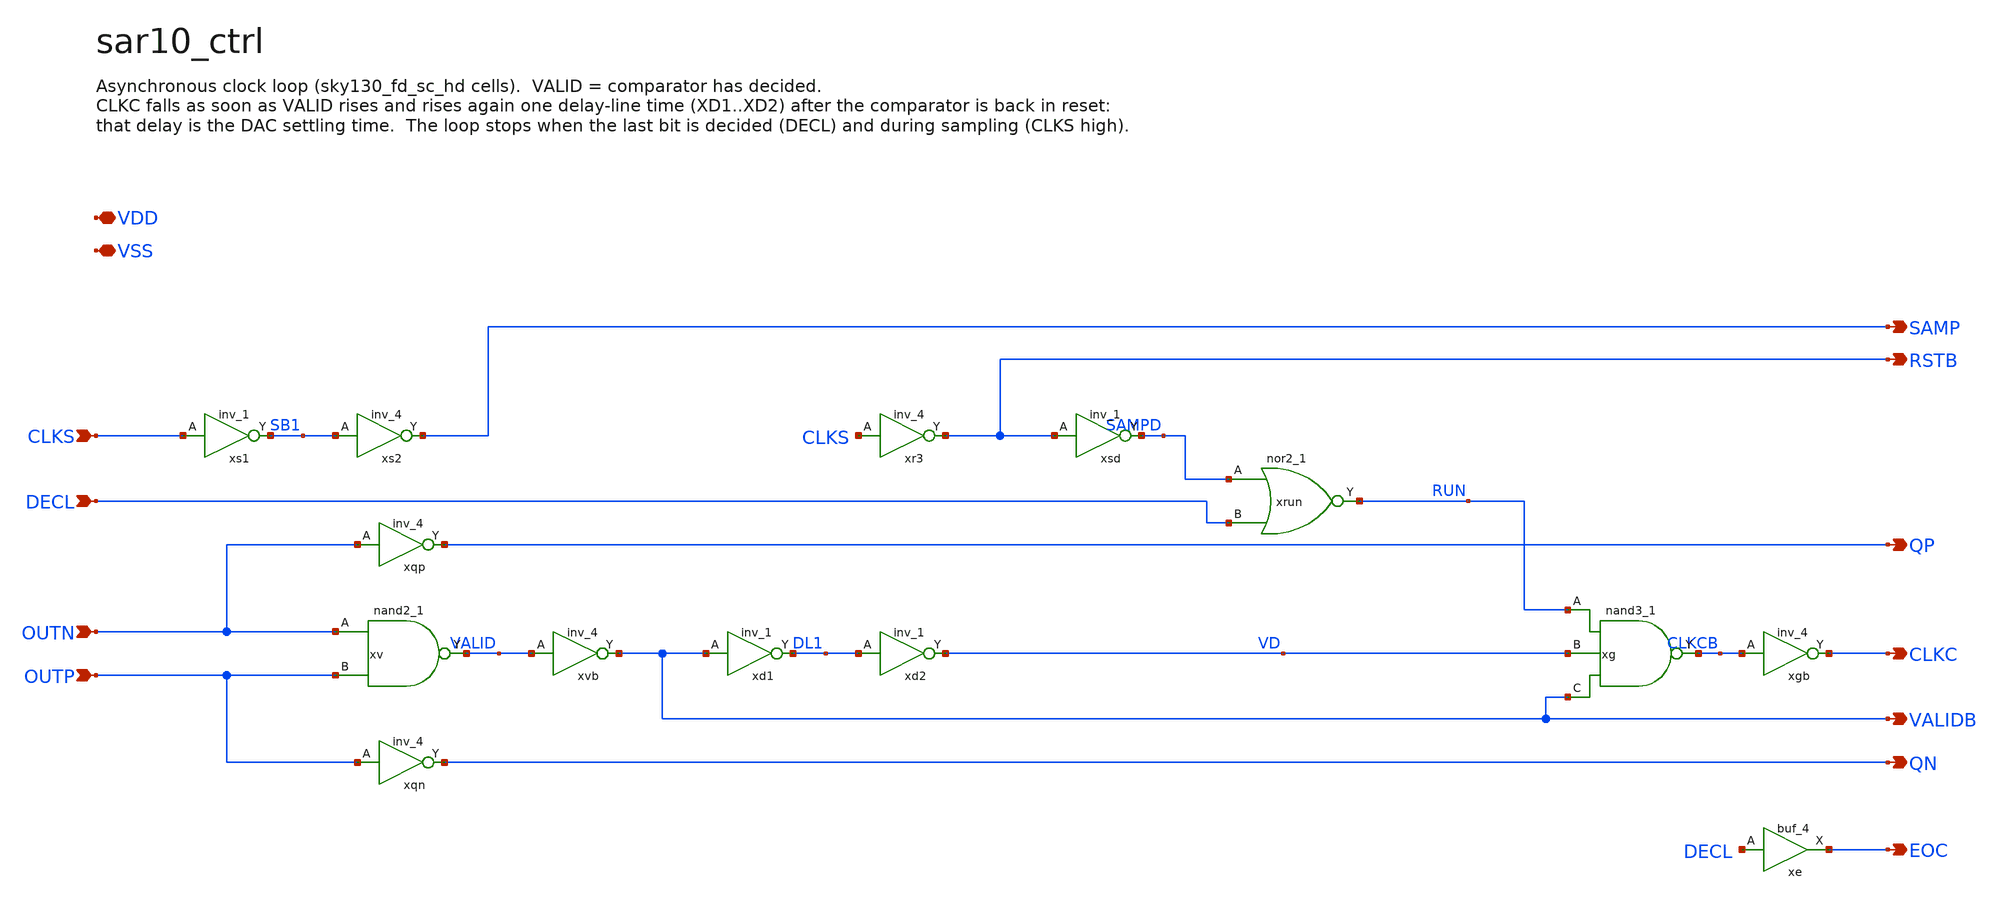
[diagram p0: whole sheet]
** sch_path: xschem/sar10_ctrl.sch
**.subckt sar10_ctrl CLKS DECL OUTN OUTP SAMP RSTB QP CLKC VALIDB QN EOC VDD VSS
*.ipin CLKS
*.ipin DECL
*.ipin OUTN
*.ipin OUTP
*.opin SAMP
*.opin RSTB
*.opin QP
*.opin CLKC
*.opin VALIDB
*.opin QN
*.opin EOC
*.iopin VDD
*.iopin VSS
xs1 CLKS VSS VSS VDD VDD SB1 sky130_fd_sc_hd__inv_1
xs2 SB1 VSS VSS VDD VDD SAMP sky130_fd_sc_hd__inv_4
xr3 CLKS VSS VSS VDD VDD RSTB sky130_fd_sc_hd__inv_4
xsd RSTB VSS VSS VDD VDD SAMPD sky130_fd_sc_hd__inv_1
xrun SAMPD DECL VSS VSS VDD VDD RUN sky130_fd_sc_hd__nor2_1
xqp OUTN VSS VSS VDD VDD QP sky130_fd_sc_hd__inv_4
xv OUTN OUTP VSS VSS VDD VDD VALID sky130_fd_sc_hd__nand2_1
xqn OUTP VSS VSS VDD VDD QN sky130_fd_sc_hd__inv_4
xvb VALID VSS VSS VDD VDD VALIDB sky130_fd_sc_hd__inv_4
xd1 VALIDB VSS VSS VDD VDD DL1 sky130_fd_sc_hd__inv_1
xd2 DL1 VSS VSS VDD VDD VD sky130_fd_sc_hd__inv_1
xg RUN VD VALIDB VSS VSS VDD VDD CLKCB sky130_fd_sc_hd__nand3_1
xgb CLKCB VSS VSS VDD VDD CLKC sky130_fd_sc_hd__inv_4
xe DECL VSS VSS VDD VDD EOC sky130_fd_sc_hd__buf_4
**.ends
.end
